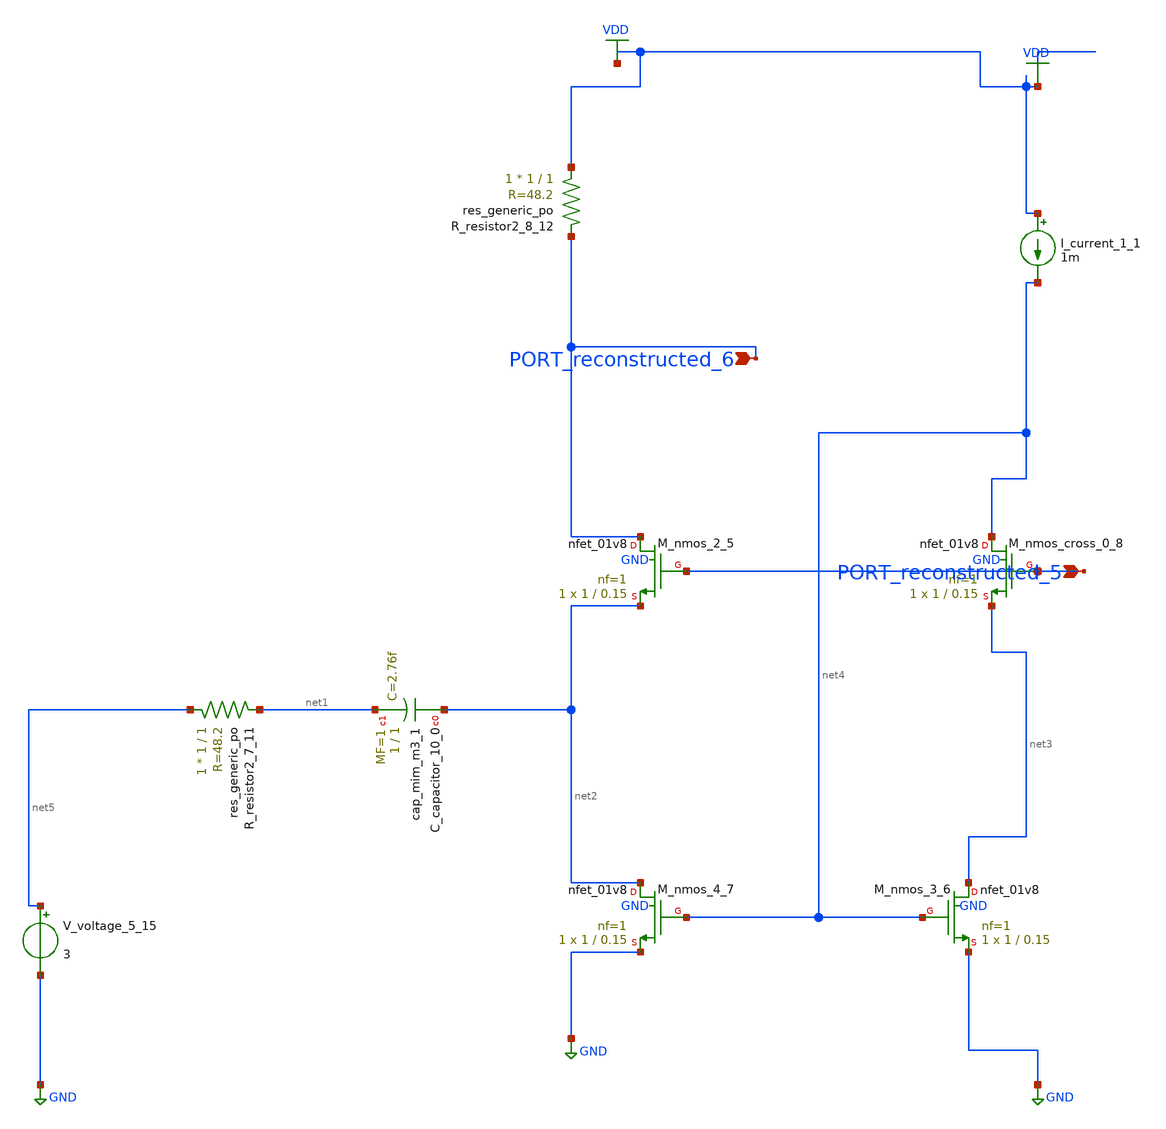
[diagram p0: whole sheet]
** sch_path: schematics/AMSNet/314.sch
**.subckt 314 PORT_reconstructed_6 PORT_reconstructed_5
*.ipin PORT_reconstructed_6
*.ipin PORT_reconstructed_5
XC_capacitor_10_0 net2 net1 sky130_fd_pr__cap_mim_m3_1 W=1 L=1 MF=1 m=1
I_current_1_1 VDD net4 1m
XM_nmos_2_5 PORT_reconstructed_6 PORT_reconstructed_5 net2 GND sky130_fd_pr__nfet_01v8 L=0.15 W=1 nf=1
+ ad='int((1 + 1)/2) * 1 / 1 * 0.29' as='int((1 + 2)/2) * 1 / 1 * 0.29' pd='2*int((1 + 1)/2) * (1 / 1 + 0.29)'
+ ps='2*int((1 + 2)/2) * (1 / 1 + 0.29)' nrd='0.29 / 1 ' nrs='0.29 / 1 ' sa=0 sb=0 sd=0 mult=1 m=1
XM_nmos_3_6 net3 net4 GND GND sky130_fd_pr__nfet_01v8 L=0.15 W=1 nf=1 ad='int((1 + 1)/2) * 1 / 1 * 0.29'
+ as='int((1 + 2)/2) * 1 / 1 * 0.29' pd='2*int((1 + 1)/2) * (1 / 1 + 0.29)' ps='2*int((1 + 2)/2) * (1 / 1 + 0.29)'
+ nrd='0.29 / 1 ' nrs='0.29 / 1 ' sa=0 sb=0 sd=0 mult=1 m=1
XM_nmos_4_7 net2 net4 GND GND sky130_fd_pr__nfet_01v8 L=0.15 W=1 nf=1 ad='int((1 + 1)/2) * 1 / 1 * 0.29'
+ as='int((1 + 2)/2) * 1 / 1 * 0.29' pd='2*int((1 + 1)/2) * (1 / 1 + 0.29)' ps='2*int((1 + 2)/2) * (1 / 1 + 0.29)'
+ nrd='0.29 / 1 ' nrs='0.29 / 1 ' sa=0 sb=0 sd=0 mult=1 m=1
XM_nmos_cross_0_8 net4 PORT_reconstructed_5 net3 GND sky130_fd_pr__nfet_01v8 L=0.15 W=1 nf=1 ad='int((1 + 1)/2) * 1 / 1 * 0.29'
+ as='int((1 + 2)/2) * 1 / 1 * 0.29' pd='2*int((1 + 1)/2) * (1 / 1 + 0.29)' ps='2*int((1 + 2)/2) * (1 / 1 + 0.29)'
+ nrd='0.29 / 1 ' nrs='0.29 / 1 ' sa=0 sb=0 sd=0 mult=1 m=1
XR_resistor2_7_11 net5 net1 sky130_fd_pr__res_generic_po W=1 L=1 m=1
XR_resistor2_8_12 VDD PORT_reconstructed_6 sky130_fd_pr__res_generic_po W=1 L=1 m=1
V_voltage_5_15 net5 GND 3
**.ends
.GLOBAL GND
.GLOBAL VDD
.end
